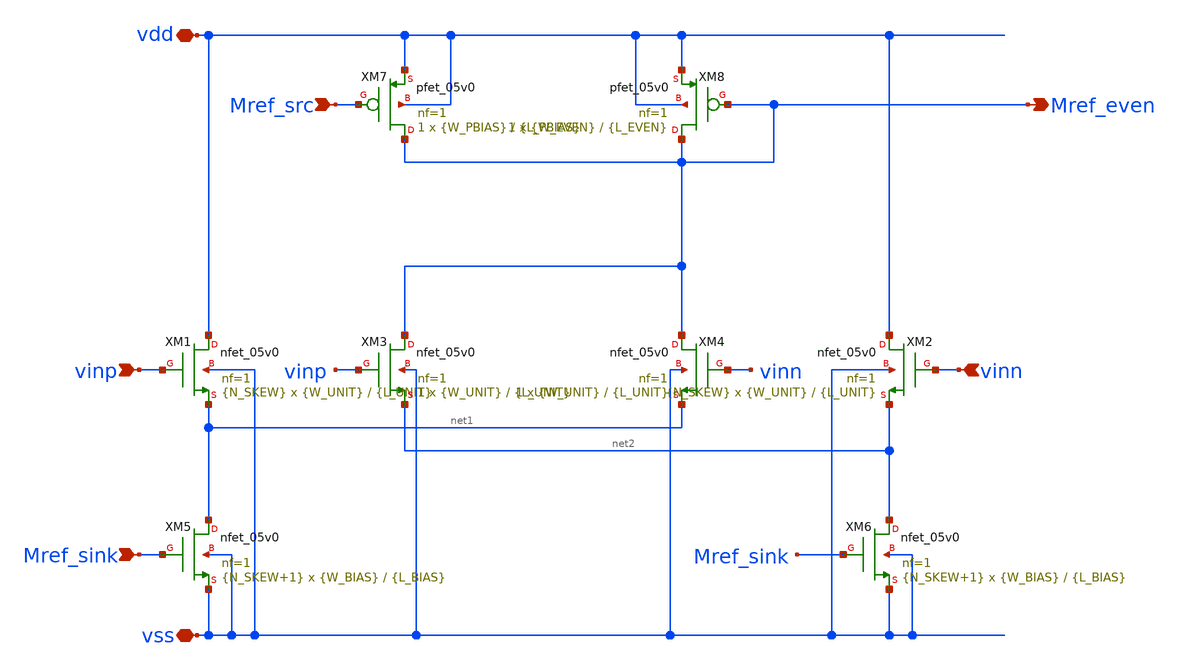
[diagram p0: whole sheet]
** sch_path: designs/libs/core_analog/quad_diff_in/quad_diff_in.sch
**.subckt quad_diff_in vdd vss vinp vinn Mref_src Mref_sink Mref_even
*.iopin vdd
*.iopin vss
*.ipin vinp
*.ipin vinn
*.ipin Mref_src
*.ipin Mref_sink
*.opin Mref_even
XM1 vdd vinp net1 vss nfet_05v0 L={L_UNIT} W={W_UNIT} nf=1 ad='int((nf+1)/2) * W/nf * 0.18u' as='int((nf+2)/2) * W/nf * 0.18u'
+ pd='2*int((nf+1)/2) * (W/nf + 0.18u)' ps='2*int((nf+2)/2) * (W/nf + 0.18u)' nrd='0.18u / W' nrs='0.18u / W'
+ sa=0 sb=0 sd=0 m={N_SKEW}
XM3 Mref_even vinp net2 vss nfet_05v0 L={L_UNIT} W={W_UNIT} nf=1 ad='int((nf+1)/2) * W/nf * 0.18u' as='int((nf+2)/2) * W/nf * 0.18u'
+ pd='2*int((nf+1)/2) * (W/nf + 0.18u)' ps='2*int((nf+2)/2) * (W/nf + 0.18u)' nrd='0.18u / W' nrs='0.18u / W'
+ sa=0 sb=0 sd=0 m=1
XM4 Mref_even vinn net1 vss nfet_05v0 L={L_UNIT} W={W_UNIT} nf=1 ad='int((nf+1)/2) * W/nf * 0.18u' as='int((nf+2)/2) * W/nf * 0.18u'
+ pd='2*int((nf+1)/2) * (W/nf + 0.18u)' ps='2*int((nf+2)/2) * (W/nf + 0.18u)' nrd='0.18u / W' nrs='0.18u / W'
+ sa=0 sb=0 sd=0 m=1
XM5 net1 Mref_sink vss vss nfet_05v0 L={L_BIAS} W={W_BIAS} nf=1 ad='int((nf+1)/2) * W/nf * 0.18u' as='int((nf+2)/2) * W/nf * 0.18u'
+ pd='2*int((nf+1)/2) * (W/nf + 0.18u)' ps='2*int((nf+2)/2) * (W/nf + 0.18u)' nrd='0.18u / W' nrs='0.18u / W'
+ sa=0 sb=0 sd=0 m={N_SKEW+1}
XM6 net2 Mref_sink vss vss nfet_05v0 L={L_BIAS} W={W_BIAS} nf=1 ad='int((nf+1)/2) * W/nf * 0.18u' as='int((nf+2)/2) * W/nf * 0.18u'
+ pd='2*int((nf+1)/2) * (W/nf + 0.18u)' ps='2*int((nf+2)/2) * (W/nf + 0.18u)' nrd='0.18u / W' nrs='0.18u / W'
+ sa=0 sb=0 sd=0 m={N_SKEW+1}
XM7 Mref_even Mref_src vdd vdd pfet_05v0 L={L_PBIAS} W={W_PBIAS} nf=1 ad='int((nf+1)/2) * W/nf * 0.18u'
+ as='int((nf+2)/2) * W/nf * 0.18u' pd='2*int((nf+1)/2) * (W/nf + 0.18u)' ps='2*int((nf+2)/2) * (W/nf + 0.18u)'
+ nrd='0.18u / W' nrs='0.18u / W' sa=0 sb=0 sd=0 m=1
XM8 Mref_even Mref_even vdd vdd pfet_05v0 L={L_EVEN} W={W_EVEN} nf=1 ad='int((nf+1)/2) * W/nf * 0.18u'
+ as='int((nf+2)/2) * W/nf * 0.18u' pd='2*int((nf+1)/2) * (W/nf + 0.18u)' ps='2*int((nf+2)/2) * (W/nf + 0.18u)'
+ nrd='0.18u / W' nrs='0.18u / W' sa=0 sb=0 sd=0 m=1
XM2 vdd vinn net2 vss nfet_05v0 L={L_UNIT} W={W_UNIT} nf=1 ad='int((nf+1)/2) * W/nf * 0.18u' as='int((nf+2)/2) * W/nf * 0.18u'
+ pd='2*int((nf+1)/2) * (W/nf + 0.18u)' ps='2*int((nf+2)/2) * (W/nf + 0.18u)' nrd='0.18u / W' nrs='0.18u / W'
+ sa=0 sb=0 sd=0 m={N_SKEW}
**.ends
.end
